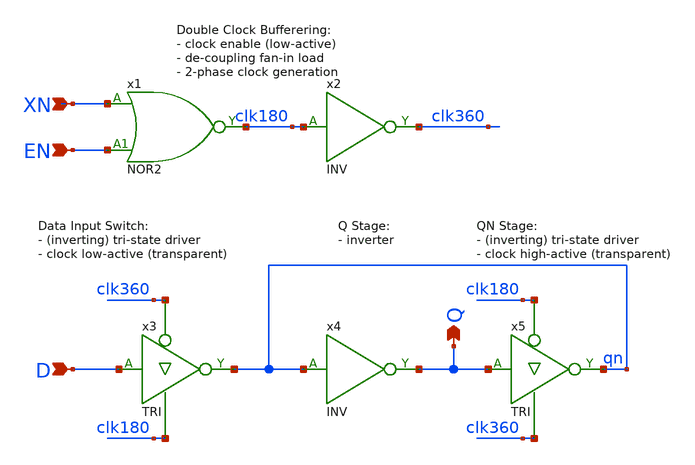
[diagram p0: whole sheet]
** sch_path: Sources/crafted/LATNE.sch
**.subckt LATNE XN D Q EN
*.ipin XN
*.ipin D
*.opin Q
*.ipin EN
x1 XN EN clk180 VDD GND NOR2 Wmin=1.5u Lmin=1u g=2 m=1
x2 clk180 clk360 VDD GND INV Wmin=1.5u Lmin=1u g=2 m=1
x3 D clk360 clk180 qn VDD GND TRI Wmin=1.5u Lmin=1u g=2 m=1
x4 qn Q VDD GND INV Wmin=1.5u Lmin=1u g=2 m=1
x5 Q clk180 clk360 qn VDD GND TRI Wmin=1.5u Lmin=1u g=2 m=1
**.ends
.end
